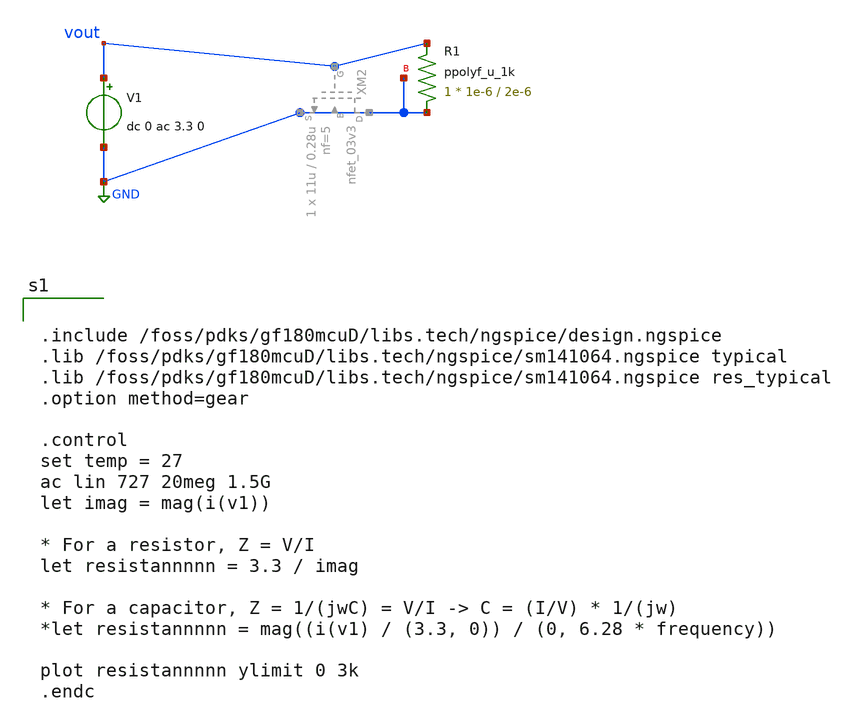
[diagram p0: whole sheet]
** sch_path: blocks/vga/test-transcap.sch
**.subckt test-transcap
V1 vout GND dc 0 ac 3.3 0
.save i(v1)
XR1 GND vout GND ppolyf_u_1k r_width=1e-6 r_length=2e-6 m=1
**** begin user architecture code


.include /foss/pdks/gf180mcuD/libs.tech/ngspice/design.ngspice
.lib /foss/pdks/gf180mcuD/libs.tech/ngspice/sm141064.ngspice typical
.lib /foss/pdks/gf180mcuD/libs.tech/ngspice/sm141064.ngspice res_typical
.option method=gear

.control
set temp = 27
ac lin 727 20meg 1.5G
let imag = mag(i(v1))

* For a resistor, Z = V/I
let resistannnnn = 3.3 / imag

* For a capacitor, Z = 1/(jwC) = V/I -> C = (I/V) * 1/(jw)
*let resistannnnn = mag((i(v1) / (3.3, 0)) / (0, 6.28 * frequency))

plot resistannnnn ylimit 0 3k
.endc


**** end user architecture code
**.ends
.GLOBAL GND
.end
